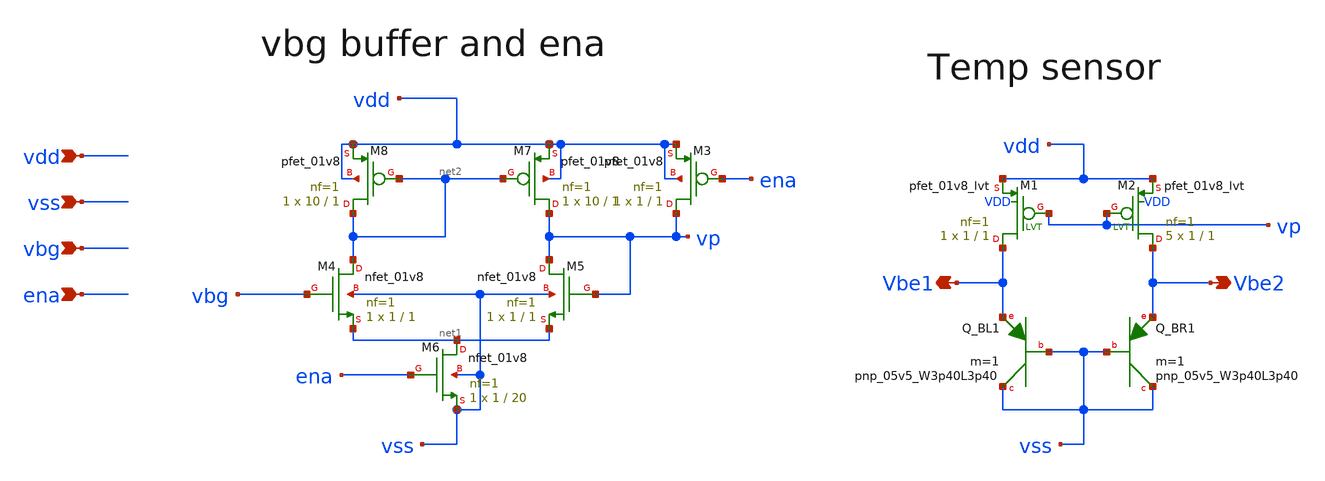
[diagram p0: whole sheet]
** sch_path: xschem/sky130_od_ip__tempsensor_ext_vp.sch
**.subckt sky130_od_ip__tempsensor_ext_vp vdd vss Vbe2 Vbe1 ena vbg
*.ipin vdd
*.ipin vss
*.opin Vbe2
*.opin Vbe1
*.ipin ena
*.ipin vbg
XQ_BL1 vss vss Vbe1 sky130_fd_pr__pnp_05v5_W3p40L3p40 m=1
XQ_BR1 vss vss Vbe2 sky130_fd_pr__pnp_05v5_W3p40L3p40 m=1
XM1 Vbe1 vp vdd VDD sky130_fd_pr__pfet_01v8_lvt L=1 W=1 nf=1 ad='int((nf+1)/2) * W/nf * 0.29' as='int((nf+2)/2) * W/nf * 0.29'
+ pd='2*int((nf+1)/2) * (W/nf + 0.29)' ps='2*int((nf+2)/2) * (W/nf + 0.29)' nrd='0.29 / W' nrs='0.29 / W'
+ sa=0 sb=0 sd=0 mult=1 m=1
XM2 Vbe2 vp vdd VDD sky130_fd_pr__pfet_01v8_lvt L=1 W=1 nf=1 ad='int((nf+1)/2) * W/nf * 0.29' as='int((nf+2)/2) * W/nf * 0.29'
+ pd='2*int((nf+1)/2) * (W/nf + 0.29)' ps='2*int((nf+2)/2) * (W/nf + 0.29)' nrd='0.29 / W' nrs='0.29 / W'
+ sa=0 sb=0 sd=0 mult=5 m=5
XM4 net2 vbg net1 vss sky130_fd_pr__nfet_01v8 L=1 W=1 nf=1 ad='int((nf+1)/2) * W/nf * 0.29' as='int((nf+2)/2) * W/nf * 0.29'
+ pd='2*int((nf+1)/2) * (W/nf + 0.29)' ps='2*int((nf+2)/2) * (W/nf + 0.29)' nrd='0.29 / W' nrs='0.29 / W'
+ sa=0 sb=0 sd=0 mult=1 m=1
XM5 vp vp net1 vss sky130_fd_pr__nfet_01v8 L=1 W=1 nf=1 ad='int((nf+1)/2) * W/nf * 0.29' as='int((nf+2)/2) * W/nf * 0.29'
+ pd='2*int((nf+1)/2) * (W/nf + 0.29)' ps='2*int((nf+2)/2) * (W/nf + 0.29)' nrd='0.29 / W' nrs='0.29 / W'
+ sa=0 sb=0 sd=0 mult=1 m=1
XM7 vp net2 vdd vdd sky130_fd_pr__pfet_01v8 L=1 W=10 nf=1 ad='int((nf+1)/2) * W/nf * 0.29' as='int((nf+2)/2) * W/nf * 0.29'
+ pd='2*int((nf+1)/2) * (W/nf + 0.29)' ps='2*int((nf+2)/2) * (W/nf + 0.29)' nrd='0.29 / W' nrs='0.29 / W'
+ sa=0 sb=0 sd=0 mult=1 m=1
XM8 net2 net2 vdd vdd sky130_fd_pr__pfet_01v8 L=1 W=10 nf=1 ad='int((nf+1)/2) * W/nf * 0.29' as='int((nf+2)/2) * W/nf * 0.29'
+ pd='2*int((nf+1)/2) * (W/nf + 0.29)' ps='2*int((nf+2)/2) * (W/nf + 0.29)' nrd='0.29 / W' nrs='0.29 / W'
+ sa=0 sb=0 sd=0 mult=1 m=1
XM3 vp ena vdd vdd sky130_fd_pr__pfet_01v8 L=1 W=1 nf=1 ad='int((nf+1)/2) * W/nf * 0.29' as='int((nf+2)/2) * W/nf * 0.29'
+ pd='2*int((nf+1)/2) * (W/nf + 0.29)' ps='2*int((nf+2)/2) * (W/nf + 0.29)' nrd='0.29 / W' nrs='0.29 / W'
+ sa=0 sb=0 sd=0 mult=1 m=1
XM6 net1 ena vss vss sky130_fd_pr__nfet_01v8 L=20 W=1 nf=1 ad='int((nf+1)/2) * W/nf * 0.29' as='int((nf+2)/2) * W/nf * 0.29'
+ pd='2*int((nf+1)/2) * (W/nf + 0.29)' ps='2*int((nf+2)/2) * (W/nf + 0.29)' nrd='0.29 / W' nrs='0.29 / W'
+ sa=0 sb=0 sd=0 mult=1 m=1
**.ends
.end
